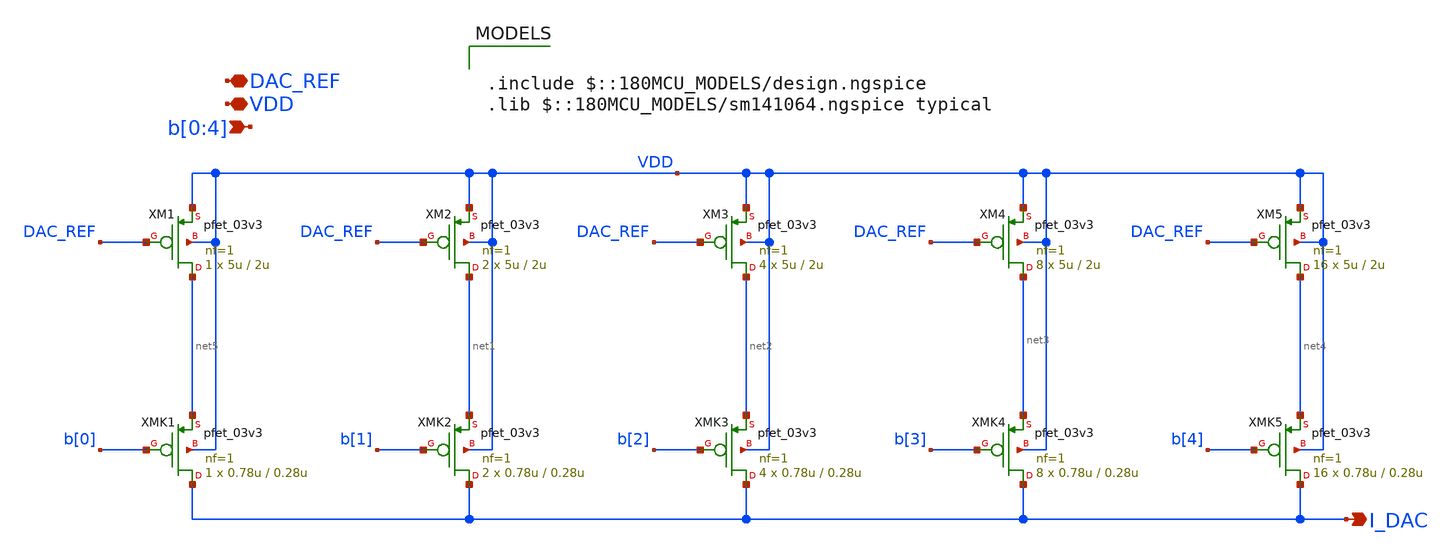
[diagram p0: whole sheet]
** sch_path: DAC_CORE_5bit/DAC_CORE_5bit.sch
**.subckt DAC_CORE_5bit I_DAC VDD DAC_REF b[0],b[1],b[2],b[3],b[4]
*.opin I_DAC
*.iopin VDD
*.iopin DAC_REF
*.ipin b[0],b[1],b[2],b[3],b[4]
XMK1 I_DAC b[0] net5 VDD pfet_03v3 L=0.28u W=0.78u nf=1 ad='int((nf+1)/2) * W/nf * 0.18u' as='int((nf+2)/2) * W/nf * 0.18u'
+ pd='2*int((nf+1)/2) * (W/nf + 0.18u)' ps='2*int((nf+2)/2) * (W/nf + 0.18u)' nrd='0.18u / W' nrs='0.18u / W'
+ sa=0 sb=0 sd=0 m=1
XMK2 I_DAC b[1] net1 VDD pfet_03v3 L=0.28u W=0.78u nf=1 ad='int((nf+1)/2) * W/nf * 0.18u' as='int((nf+2)/2) * W/nf * 0.18u'
+ pd='2*int((nf+1)/2) * (W/nf + 0.18u)' ps='2*int((nf+2)/2) * (W/nf + 0.18u)' nrd='0.18u / W' nrs='0.18u / W'
+ sa=0 sb=0 sd=0 m=2
XMK3 I_DAC b[2] net2 VDD pfet_03v3 L=0.28u W=0.78u nf=1 ad='int((nf+1)/2) * W/nf * 0.18u' as='int((nf+2)/2) * W/nf * 0.18u'
+ pd='2*int((nf+1)/2) * (W/nf + 0.18u)' ps='2*int((nf+2)/2) * (W/nf + 0.18u)' nrd='0.18u / W' nrs='0.18u / W'
+ sa=0 sb=0 sd=0 m=4
XMK4 I_DAC b[3] net3 VDD pfet_03v3 L=0.28u W=0.78u nf=1 ad='int((nf+1)/2) * W/nf * 0.18u' as='int((nf+2)/2) * W/nf * 0.18u'
+ pd='2*int((nf+1)/2) * (W/nf + 0.18u)' ps='2*int((nf+2)/2) * (W/nf + 0.18u)' nrd='0.18u / W' nrs='0.18u / W'
+ sa=0 sb=0 sd=0 m=8
XMK5 I_DAC b[4] net4 VDD pfet_03v3 L=0.28u W=0.78u nf=1 ad='int((nf+1)/2) * W/nf * 0.18u' as='int((nf+2)/2) * W/nf * 0.18u'
+ pd='2*int((nf+1)/2) * (W/nf + 0.18u)' ps='2*int((nf+2)/2) * (W/nf + 0.18u)' nrd='0.18u / W' nrs='0.18u / W'
+ sa=0 sb=0 sd=0 m=16
XM1 net5 DAC_REF VDD VDD pfet_03v3 L=2u W=5u nf=1 ad='int((nf+1)/2) * W/nf * 0.18u' as='int((nf+2)/2) * W/nf * 0.18u'
+ pd='2*int((nf+1)/2) * (W/nf + 0.18u)' ps='2*int((nf+2)/2) * (W/nf + 0.18u)' nrd='0.18u / W' nrs='0.18u / W'
+ sa=0 sb=0 sd=0 m=1
XM2 net1 DAC_REF VDD VDD pfet_03v3 L=2u W=5u nf=1 ad='int((nf+1)/2) * W/nf * 0.18u' as='int((nf+2)/2) * W/nf * 0.18u'
+ pd='2*int((nf+1)/2) * (W/nf + 0.18u)' ps='2*int((nf+2)/2) * (W/nf + 0.18u)' nrd='0.18u / W' nrs='0.18u / W'
+ sa=0 sb=0 sd=0 m=2
XM3 net2 DAC_REF VDD VDD pfet_03v3 L=2u W=5u nf=1 ad='int((nf+1)/2) * W/nf * 0.18u' as='int((nf+2)/2) * W/nf * 0.18u'
+ pd='2*int((nf+1)/2) * (W/nf + 0.18u)' ps='2*int((nf+2)/2) * (W/nf + 0.18u)' nrd='0.18u / W' nrs='0.18u / W'
+ sa=0 sb=0 sd=0 m=4
XM4 net3 DAC_REF VDD VDD pfet_03v3 L=2u W=5u nf=1 ad='int((nf+1)/2) * W/nf * 0.18u' as='int((nf+2)/2) * W/nf * 0.18u'
+ pd='2*int((nf+1)/2) * (W/nf + 0.18u)' ps='2*int((nf+2)/2) * (W/nf + 0.18u)' nrd='0.18u / W' nrs='0.18u / W'
+ sa=0 sb=0 sd=0 m=8
XM5 net4 DAC_REF VDD VDD pfet_03v3 L=2u W=5u nf=1 ad='int((nf+1)/2) * W/nf * 0.18u' as='int((nf+2)/2) * W/nf * 0.18u'
+ pd='2*int((nf+1)/2) * (W/nf + 0.18u)' ps='2*int((nf+2)/2) * (W/nf + 0.18u)' nrd='0.18u / W' nrs='0.18u / W'
+ sa=0 sb=0 sd=0 m=16
**** begin user architecture code

.include $::180MCU_MODELS/design.ngspice
.lib $::180MCU_MODELS/sm141064.ngspice typical

**** end user architecture code
**.ends
.end
